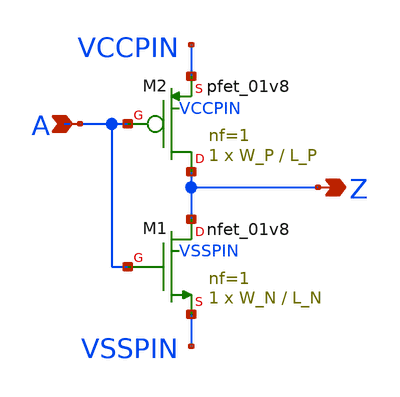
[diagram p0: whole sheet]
** sch_path: skywater-tests/yinv.sch
**.subckt yinv A Z
*.ipin A
*.opin Z
XM1 Z A VSSPIN VSSPIN sky130_fd_pr__nfet_01v8 L=L_N W=W_N nf=1 ad='int((nf+1)/2) * W/nf * 0.29' as='int((nf+2)/2) * W/nf * 0.29'
+ pd='2*int((nf+1)/2) * (W/nf + 0.29)' ps='2*int((nf+2)/2) * (W/nf + 0.29)' nrd='0.29 / W' nrs='0.29 / W'
+ sa=0 sb=0 sd=0 mult=1 m=1
XM2 Z A VCCPIN VCCPIN sky130_fd_pr__pfet_01v8 L=L_P W=W_P nf=1 ad='int((nf+1)/2) * W/nf * 0.29' as='int((nf+2)/2) * W/nf * 0.29'
+ pd='2*int((nf+1)/2) * (W/nf + 0.29)' ps='2*int((nf+2)/2) * (W/nf + 0.29)' nrd='0.29 / W' nrs='0.29 / W'
+ sa=0 sb=0 sd=0 mult=1 m=1
**.ends
.end
